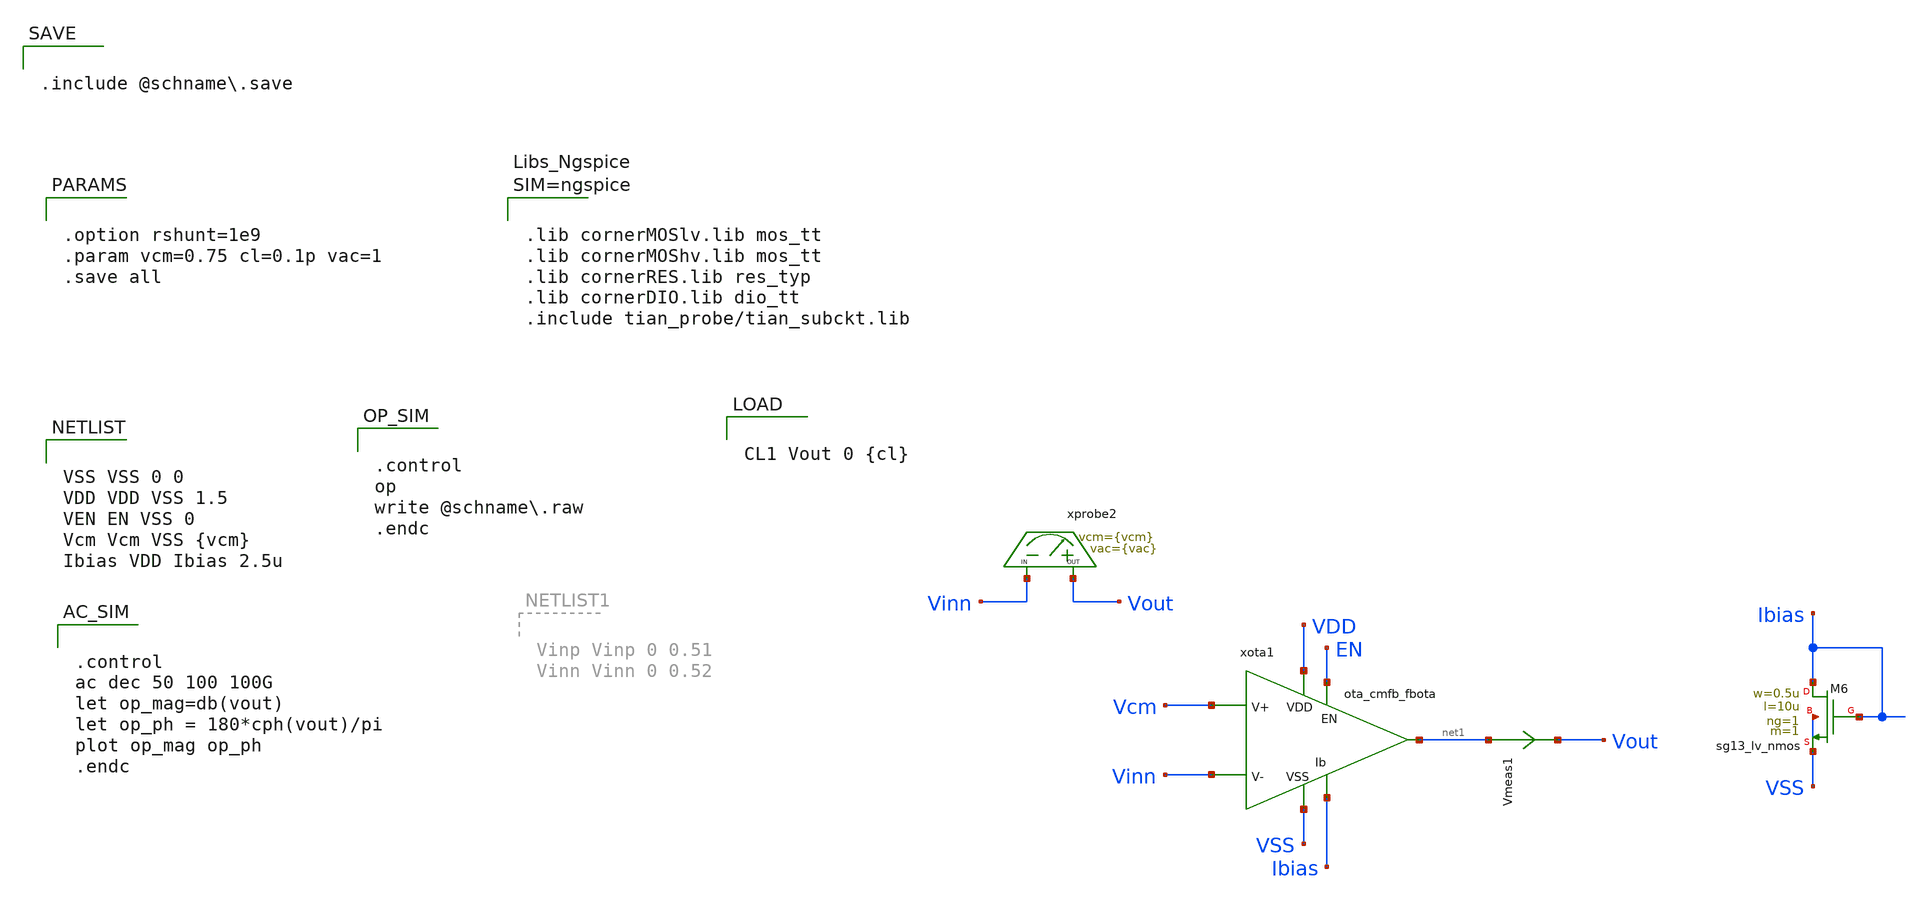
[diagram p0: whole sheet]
** sch_path: schema/ota_cmfb_fbota/ota_cmfb_fbota_tb.sch
**.subckt ota_cmfb_fbota_tb
Vmeas1 net1 Vout 0
.save i(vmeas1)
xprobe2 Vout Vinn ac_probe vcm={vcm} vac={vac}
xota1 VDD EN Ibias Vinn Vcm net1 VSS ota_cmfb_fbota
XM6 Ibias Ibias VSS VSS sg13_lv_nmos w=0.5u l=10u ng=1 m=1 mm_ok=1
**** begin user architecture code


VSS VSS 0 0
VDD VDD VSS 1.5
VEN EN VSS 0
Vcm Vcm VSS {vcm}
Ibias VDD Ibias 2.5u



.control
op
write @schname.raw
.endc




.lib cornerMOSlv.lib mos_tt
.lib cornerMOShv.lib mos_tt
.lib cornerRES.lib res_typ
.lib cornerDIO.lib dio_tt
.include tian_probe/tian_subckt.lib





.control
ac dec 50 100 100G
let op_mag=db(vout)
let op_ph = 180*cph(vout)/pi
plot op_mag op_ph
.endc




.option rshunt=1e9
.param vcm=0.75 cl=0.1p vac=1
.save all




CL1 Vout 0 {cl}



.include @schname.save

**** end user architecture code
**.ends

* expanding   symbol:  ac_probe/ac_probe.sym # of pins=2
** sym_path: schema/ac_probe/ac_probe.sym
** sch_path: schema/ac_probe/ac_probe.sch
.subckt ac_probe OUT IN  vcm=0.75 vac=0.01

*.iopin IN
*.iopin OUT
C1 0 IN 1 m=1
V1 IN 0 {vcm} ac {vac}
R1 OUT IN 1G m=1
.ends


* expanding   symbol:  ota_cmfb_fbota/ota_cmfb_fbota.sym # of pins=7
** sym_path: schema/ota_cmfb_fbota/ota_cmfb_fbota.sym
** sch_path: schema/ota_cmfb_fbota/ota_cmfb_fbota.sch
.subckt ota_cmfb_fbota VDD EN Ibias Vinn Vinp Vout VSS
*.opin Vout
*.iopin VDD
*.iopin VSS
*.ipin Vinp
*.ipin Ibias
*.ipin Vinn
*.ipin EN
XMJ Vout mirror VSS VSS sg13_lv_nmos w=0.25u l=10u ng=1 m=4 mm_ok=1
XML Vout Vinn src_kl VDD sg13_lv_pmos w=2.5u l=2u ng=1 m=2 mm_ok=1
XMI mirror mirror VSS VSS sg13_lv_nmos w=0.25u l=10u ng=1 m=4 mm_ok=1
XMK mirror Vinp src_kl VDD sg13_lv_pmos w=2.5u l=2u ng=1 m=2 mm_ok=1
XMO src_kl tail_bias VDD VDD sg13_lv_pmos w=1.25u l=5u ng=1 m=8 mm_ok=1
XMN VDD tail_bias tail_bias VDD sg13_lv_pmos w=1.25u l=5u ng=1 m=2 mm_ok=1
XMH tail_bias Ibias VSS VSS sg13_lv_nmos w=0.25u l=10u ng=1 m=2 mm_ok=1
XMN1 mirror EN_N VSS VSS sg13_lv_nmos w=740.00n l=130.00n ng=1 m=1 mm_ok=1
XM2 VSS VSS tail_bias VSS sg13_lv_nmos w=0.25u l=0.5u ng=1 m=2 mm_ok=1
XMK1 mirror VDD VDD VDD sg13_lv_pmos w=2.5u l=0.5u ng=1 m=1 mm_ok=1
XMK2 Vout VDD VDD VDD sg13_lv_pmos w=2.5u l=0.5u ng=1 m=1 mm_ok=1
XMK3 src_kl VDD VDD VDD sg13_lv_pmos w=2.5u l=0.5u ng=1 m=2 mm_ok=1
XMK4 tail_bias VDD VDD VDD sg13_lv_pmos w=1.25u l=0.5u ng=1 m=2 mm_ok=1
XMN0 EN_N EN VSS VSS sg13_lv_nmos w=2.96u l=130.00n ng=1 m=1 mm_ok=1
XMP0 EN_N EN VDD VDD sg13_lv_pmos w=4.48u l=130.00n ng=1 m=1 mm_ok=1
.ends

.end
